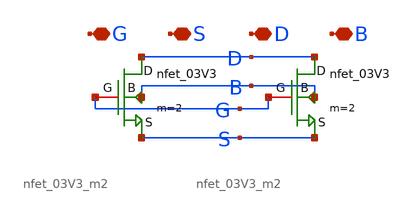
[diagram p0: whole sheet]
** sch_path: DAC_PAKISTAN_01/Pakistan1_Xschem/nfet_03V3_m4.sch
**.subckt nfet_03V3_m4 G S D B
*.iopin G
*.iopin S
*.iopin D
*.iopin B
x1 S D B G nfet_03V3_m2
x2 S D B G nfet_03V3_m2
**.ends
.end
